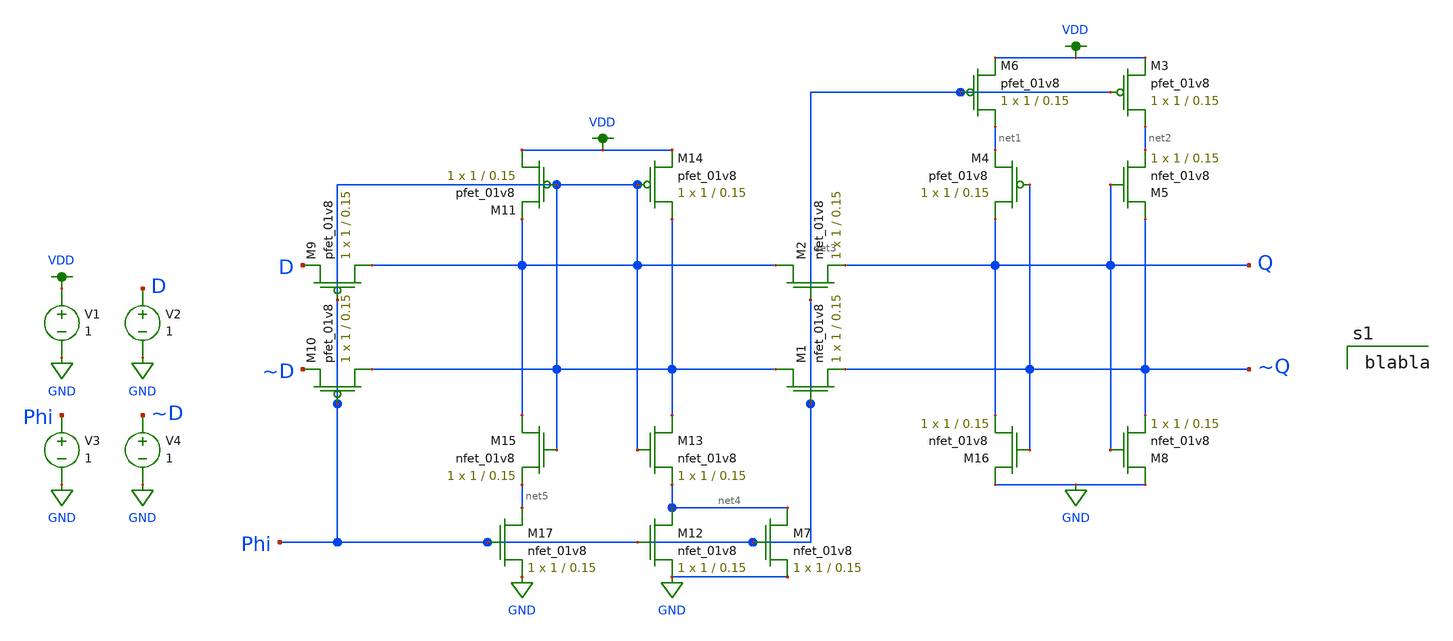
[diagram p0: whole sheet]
** sch_path: shift register/Schematic/1_bit_shift_register_3tdevices.sch
**.subckt 1_bit_shift_register_3tdevices
XM17 net5 Phi GND GND sky130_fd_pr__nfet_01v8 L=0.15 W=1 nf=1 ad='int((nf+1)/2) * W/nf * 0.29' as='int((nf+2)/2) * W/nf * 0.29'
+ pd='2*int((nf+1)/2) * (W/nf + 0.29)' ps='2*int((nf+2)/2) * (W/nf + 0.29)' nrd='0.29 / W' nrs='0.29 / W'
+ sa=0 sb=0 sd=0 mult=1 m=1
XM12 net4 Phi GND GND sky130_fd_pr__nfet_01v8 L=0.15 W=1 nf=1 ad='int((nf+1)/2) * W/nf * 0.29' as='int((nf+2)/2) * W/nf * 0.29'
+ pd='2*int((nf+1)/2) * (W/nf + 0.29)' ps='2*int((nf+2)/2) * (W/nf + 0.29)' nrd='0.29 / W' nrs='0.29 / W'
+ sa=0 sb=0 sd=0 mult=1 m=1
XM13 Phi Phi net4 GND sky130_fd_pr__nfet_01v8 L=0.15 W=1 nf=1 ad='int((nf+1)/2) * W/nf * 0.29' as='int((nf+2)/2) * W/nf * 0.29'
+ pd='2*int((nf+1)/2) * (W/nf + 0.29)' ps='2*int((nf+2)/2) * (W/nf + 0.29)' nrd='0.29 / W' nrs='0.29 / W'
+ sa=0 sb=0 sd=0 mult=1 m=1
XM15 Phi Phi net5 GND sky130_fd_pr__nfet_01v8 L=0.15 W=1 nf=1 ad='int((nf+1)/2) * W/nf * 0.29' as='int((nf+2)/2) * W/nf * 0.29'
+ pd='2*int((nf+1)/2) * (W/nf + 0.29)' ps='2*int((nf+2)/2) * (W/nf + 0.29)' nrd='0.29 / W' nrs='0.29 / W'
+ sa=0 sb=0 sd=0 mult=1 m=1
XM1 Phi net3 ~Q GND sky130_fd_pr__nfet_01v8 L=0.15 W=1 nf=1 ad='int((nf+1)/2) * W/nf * 0.29' as='int((nf+2)/2) * W/nf * 0.29'
+ pd='2*int((nf+1)/2) * (W/nf + 0.29)' ps='2*int((nf+2)/2) * (W/nf + 0.29)' nrd='0.29 / W' nrs='0.29 / W'
+ sa=0 sb=0 sd=0 mult=1 m=1
XM2 Phi net3 Q GND sky130_fd_pr__nfet_01v8 L=0.15 W=1 nf=1 ad='int((nf+1)/2) * W/nf * 0.29' as='int((nf+2)/2) * W/nf * 0.29'
+ pd='2*int((nf+1)/2) * (W/nf + 0.29)' ps='2*int((nf+2)/2) * (W/nf + 0.29)' nrd='0.29 / W' nrs='0.29 / W'
+ sa=0 sb=0 sd=0 mult=1 m=1
XM8 GND Q ~Q GND sky130_fd_pr__nfet_01v8 L=0.15 W=1 nf=1 ad='int((nf+1)/2) * W/nf * 0.29' as='int((nf+2)/2) * W/nf * 0.29'
+ pd='2*int((nf+1)/2) * (W/nf + 0.29)' ps='2*int((nf+2)/2) * (W/nf + 0.29)' nrd='0.29 / W' nrs='0.29 / W'
+ sa=0 sb=0 sd=0 mult=1 m=1
V1 VDD GND 1
V2 D GND 1
V3 Phi GND 1
V4 ~D GND 1
XM4 Q ~Q net1 VDD sky130_fd_pr__pfet_01v8 L=0.15 W=1 nf=1 ad='int((nf+1)/2) * W/nf * 0.29' as='int((nf+2)/2) * W/nf * 0.29'
+ pd='2*int((nf+1)/2) * (W/nf + 0.29)' ps='2*int((nf+2)/2) * (W/nf + 0.29)' nrd='0.29 / W' nrs='0.29 / W'
+ sa=0 sb=0 sd=0 mult=1 m=1
XM3 net2 net3 VDD VDD sky130_fd_pr__pfet_01v8 L=0.15 W=1 nf=1 ad='int((nf+1)/2) * W/nf * 0.29' as='int((nf+2)/2) * W/nf * 0.29'
+ pd='2*int((nf+1)/2) * (W/nf + 0.29)' ps='2*int((nf+2)/2) * (W/nf + 0.29)' nrd='0.29 / W' nrs='0.29 / W'
+ sa=0 sb=0 sd=0 mult=1 m=1
XM6 net1 net3 VDD VDD sky130_fd_pr__pfet_01v8 L=0.15 W=1 nf=1 ad='int((nf+1)/2) * W/nf * 0.29' as='int((nf+2)/2) * W/nf * 0.29'
+ pd='2*int((nf+1)/2) * (W/nf + 0.29)' ps='2*int((nf+2)/2) * (W/nf + 0.29)' nrd='0.29 / W' nrs='0.29 / W'
+ sa=0 sb=0 sd=0 mult=1 m=1
XM10 Phi Phi ~D VDD sky130_fd_pr__pfet_01v8 L=0.15 W=1 nf=1 ad='int((nf+1)/2) * W/nf * 0.29' as='int((nf+2)/2) * W/nf * 0.29'
+ pd='2*int((nf+1)/2) * (W/nf + 0.29)' ps='2*int((nf+2)/2) * (W/nf + 0.29)' nrd='0.29 / W' nrs='0.29 / W'
+ sa=0 sb=0 sd=0 mult=1 m=1
XM9 Phi Phi D VDD sky130_fd_pr__pfet_01v8 L=0.15 W=1 nf=1 ad='int((nf+1)/2) * W/nf * 0.29' as='int((nf+2)/2) * W/nf * 0.29'
+ pd='2*int((nf+1)/2) * (W/nf + 0.29)' ps='2*int((nf+2)/2) * (W/nf + 0.29)' nrd='0.29 / W' nrs='0.29 / W'
+ sa=0 sb=0 sd=0 mult=1 m=1
XM11 VDD Phi Phi VDD sky130_fd_pr__pfet_01v8 L=0.15 W=1 nf=1 ad='int((nf+1)/2) * W/nf * 0.29' as='int((nf+2)/2) * W/nf * 0.29'
+ pd='2*int((nf+1)/2) * (W/nf + 0.29)' ps='2*int((nf+2)/2) * (W/nf + 0.29)' nrd='0.29 / W' nrs='0.29 / W'
+ sa=0 sb=0 sd=0 mult=1 m=1
XM14 Phi Phi VDD VDD sky130_fd_pr__pfet_01v8 L=0.15 W=1 nf=1 ad='int((nf+1)/2) * W/nf * 0.29' as='int((nf+2)/2) * W/nf * 0.29'
+ pd='2*int((nf+1)/2) * (W/nf + 0.29)' ps='2*int((nf+2)/2) * (W/nf + 0.29)' nrd='0.29 / W' nrs='0.29 / W'
+ sa=0 sb=0 sd=0 mult=1 m=1
XM16 GND ~Q Q GND sky130_fd_pr__nfet_01v8 L=0.15 W=1 nf=1 ad='int((nf+1)/2) * W/nf * 0.29' as='int((nf+2)/2) * W/nf * 0.29'
+ pd='2*int((nf+1)/2) * (W/nf + 0.29)' ps='2*int((nf+2)/2) * (W/nf + 0.29)' nrd='0.29 / W' nrs='0.29 / W'
+ sa=0 sb=0 sd=0 mult=1 m=1
XM5 ~Q Q net2 GND sky130_fd_pr__nfet_01v8 L=0.15 W=1 nf=1 ad='int((nf+1)/2) * W/nf * 0.29' as='int((nf+2)/2) * W/nf * 0.29'
+ pd='2*int((nf+1)/2) * (W/nf + 0.29)' ps='2*int((nf+2)/2) * (W/nf + 0.29)' nrd='0.29 / W' nrs='0.29 / W'
+ sa=0 sb=0 sd=0 mult=1 m=1
XM7 net4 net3 GND GND sky130_fd_pr__nfet_01v8 L=0.15 W=1 nf=1 ad='int((nf+1)/2) * W/nf * 0.29' as='int((nf+2)/2) * W/nf * 0.29'
+ pd='2*int((nf+1)/2) * (W/nf + 0.29)' ps='2*int((nf+2)/2) * (W/nf + 0.29)' nrd='0.29 / W' nrs='0.29 / W'
+ sa=0 sb=0 sd=0 mult=1 m=1
**** begin user architecture code

.option wnflag=1
.lib ~/skywater/skywater-pdk/libraries/sky130_fd_pr_ngspice/latest/models/sky130.lib.spice sf


blabla

**** end user architecture code
**.ends
.GLOBAL GND
.GLOBAL VDD
.end
